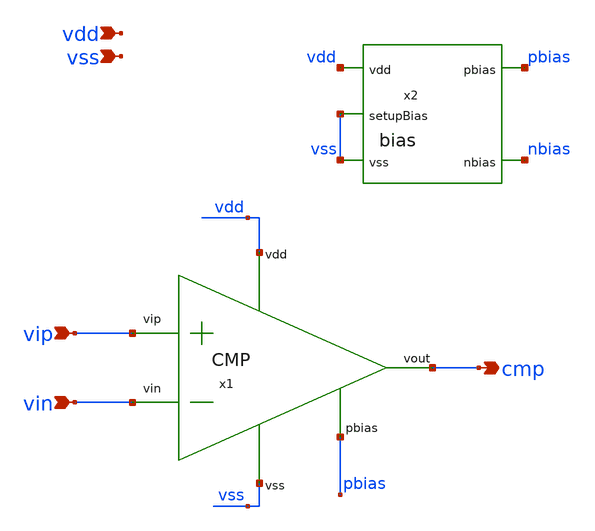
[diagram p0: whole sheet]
** sch_path: design/JNW_AVV_SKY130A/TB_CMP.sch
**.subckt TB_CMP vdd vss vip vin cmp
*.ipin vdd
*.ipin vss
*.ipin vip
*.ipin vin
*.opin cmp
x1 vdd pbias cmp vin vip vss CMP
x2 pbias vdd nbias vss vss bias
**.ends
.end
